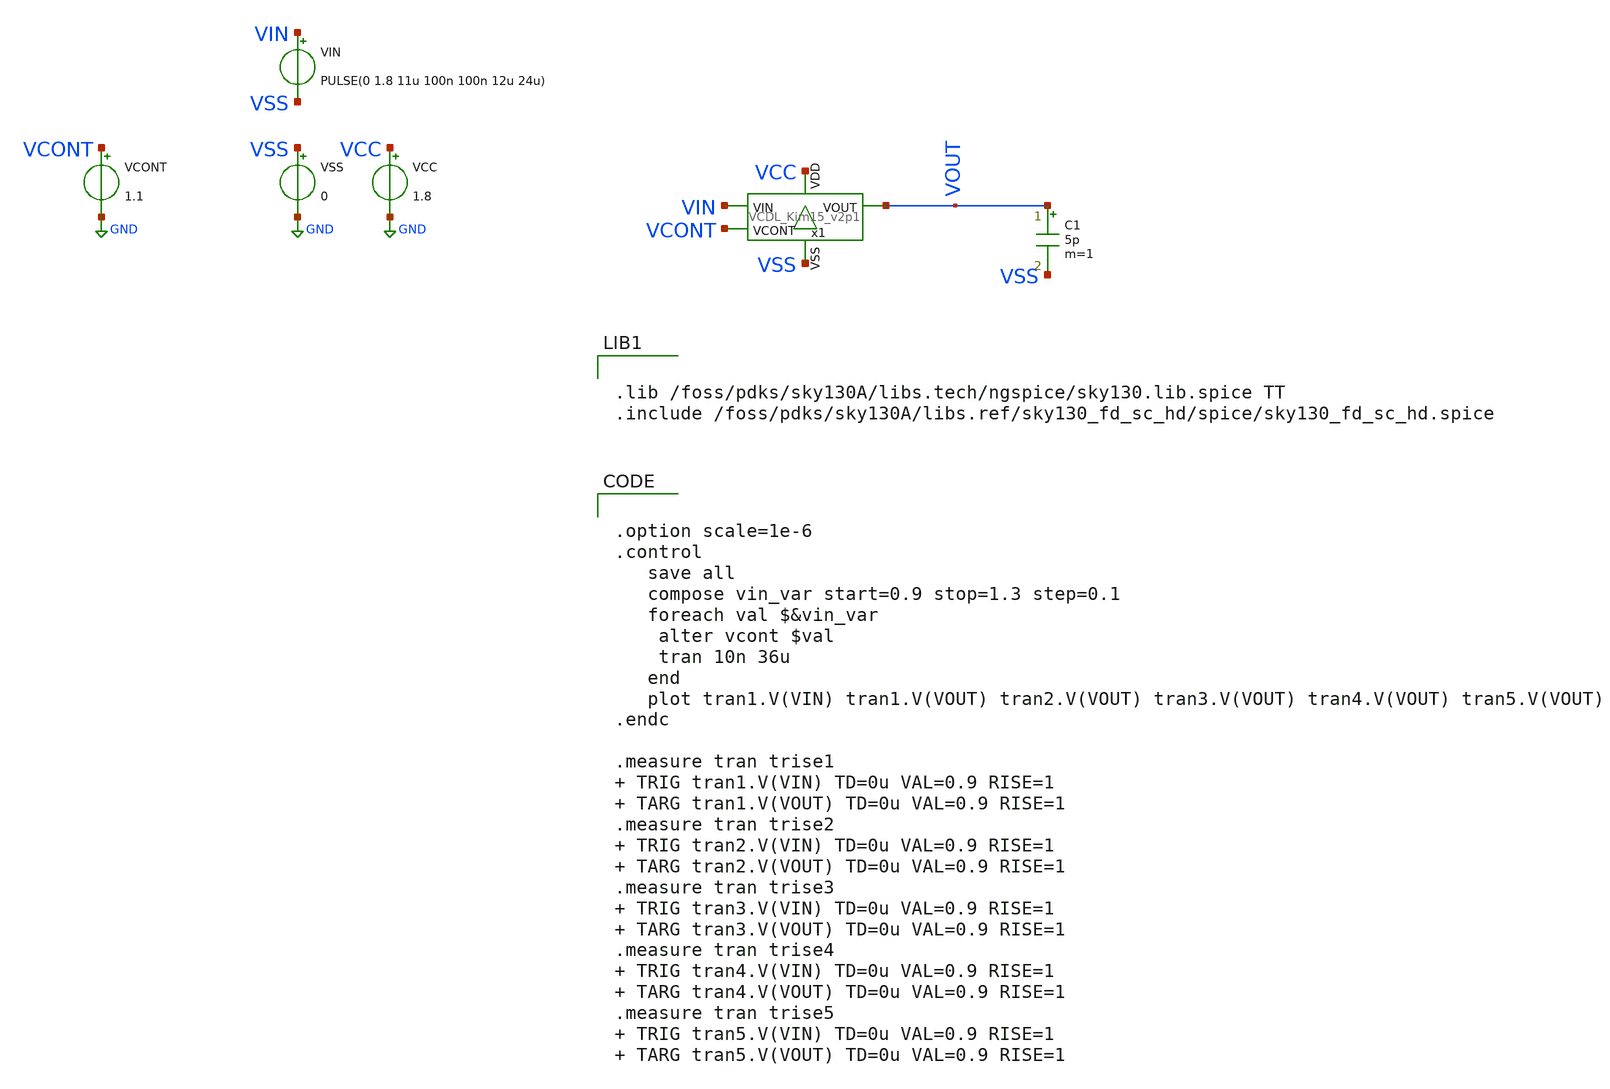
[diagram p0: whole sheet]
** sch_path: xschem/tb_VCDL_Kim_v2p1.sch
**.subckt tb_VCDL_Kim_v2p1
VCC VCC GND 1.8
VSS VSS GND 0
VIN VIN VSS PULSE(0 1.8 11u 100n 100n 12u 24u)
VCONT VCONT GND 1.1
C1 VOUT VSS 5p m=1
x1 VCC VCONT VOUT VIN VSS VCDL_Kim15_v2p1
**** begin user architecture code


.lib /foss/pdks/sky130A/libs.tech/ngspice/sky130.lib.spice TT
.include /foss/pdks/sky130A/libs.ref/sky130_fd_sc_hd/spice/sky130_fd_sc_hd.spice




.option scale=1e-6
.control
   save all
   compose vin_var start=0.9 stop=1.3 step=0.1
   foreach val $&vin_var
	alter vcont $val
	tran 10n 36u
   end
   plot tran1.V(VIN) tran1.V(VOUT) tran2.V(VOUT) tran3.V(VOUT) tran4.V(VOUT) tran5.V(VOUT)
.endc

.measure tran trise1   TRIG tran1.V(VIN) TD=0u VAL=0.9 RISE=1  TARG tran1.V(VOUT) TD=0u VAL=0.9
+ RISE=1
.measure tran trise2  TRIG tran2.V(VIN) TD=0u VAL=0.9 RISE=1  TARG tran2.V(VOUT) TD=0u VAL=0.9
+ RISE=1
.measure tran trise3  TRIG tran3.V(VIN) TD=0u VAL=0.9 RISE=1  TARG tran3.V(VOUT) TD=0u VAL=0.9
+ RISE=1
.measure tran trise4  TRIG tran4.V(VIN) TD=0u VAL=0.9 RISE=1  TARG tran4.V(VOUT) TD=0u VAL=0.9
+ RISE=1
.measure tran trise5  TRIG tran5.V(VIN) TD=0u VAL=0.9 RISE=1  TARG tran5.V(VOUT) TD=0u VAL=0.9
+ RISE=1


**** end user architecture code
**.ends

* expanding   symbol:  /foss/designs/TO202406_CMOSVCO_Esm22/xschem/VCDL_Kim15_v2p1.sym # of pins=5
** sym_path: xschem/VCDL_Kim15_v2p1.sym
** sch_path: xschem/VCDL_Kim15_v2p1.sch
.subckt VCDL_Kim15_v2p1 VDD VCONT VOUT VIN VSS
*.ipin VIN
*.opin VOUT
*.iopin VSS
*.ipin VCONT
*.iopin VDD
XM1 net2 net1 VSS VSS sky130_fd_pr__nfet_01v8 L=5 W=2 nf=1 ad='int((nf+1)/2) * W/nf * 0.29' as='int((nf+2)/2) * W/nf * 0.29'
+ pd='2*int((nf+1)/2) * (W/nf + 0.29)' ps='2*int((nf+2)/2) * (W/nf + 0.29)' nrd='0.29 / W' nrs='0.29 / W'
+ sa=0 sb=0 sd=0 mult=1 m=1
XM2 net2 net1 VCONT VCONT sky130_fd_pr__pfet_01v8 L=5 W=5 nf=1 ad='int((nf+1)/2) * W/nf * 0.29' as='int((nf+2)/2) * W/nf * 0.29'
+ pd='2*int((nf+1)/2) * (W/nf + 0.29)' ps='2*int((nf+2)/2) * (W/nf + 0.29)' nrd='0.29 / W' nrs='0.29 / W'
+ sa=0 sb=0 sd=0 mult=1 m=1
XM3 net3 net2 VSS VSS sky130_fd_pr__nfet_01v8 L=5 W=2 nf=1 ad='int((nf+1)/2) * W/nf * 0.29' as='int((nf+2)/2) * W/nf * 0.29'
+ pd='2*int((nf+1)/2) * (W/nf + 0.29)' ps='2*int((nf+2)/2) * (W/nf + 0.29)' nrd='0.29 / W' nrs='0.29 / W'
+ sa=0 sb=0 sd=0 mult=1 m=1
XM5 net3 net2 VCONT VCONT sky130_fd_pr__pfet_01v8 L=5 W=5 nf=1 ad='int((nf+1)/2) * W/nf * 0.29' as='int((nf+2)/2) * W/nf * 0.29'
+ pd='2*int((nf+1)/2) * (W/nf + 0.29)' ps='2*int((nf+2)/2) * (W/nf + 0.29)' nrd='0.29 / W' nrs='0.29 / W'
+ sa=0 sb=0 sd=0 mult=1 m=1
XM6 net1 net4 VSS VSS sky130_fd_pr__nfet_01v8 L=5 W=2 nf=1 ad='int((nf+1)/2) * W/nf * 0.29' as='int((nf+2)/2) * W/nf * 0.29'
+ pd='2*int((nf+1)/2) * (W/nf + 0.29)' ps='2*int((nf+2)/2) * (W/nf + 0.29)' nrd='0.29 / W' nrs='0.29 / W'
+ sa=0 sb=0 sd=0 mult=1 m=1
XM7 net1 net4 VCONT VCONT sky130_fd_pr__pfet_01v8 L=5 W=5 nf=1 ad='int((nf+1)/2) * W/nf * 0.29' as='int((nf+2)/2) * W/nf * 0.29'
+ pd='2*int((nf+1)/2) * (W/nf + 0.29)' ps='2*int((nf+2)/2) * (W/nf + 0.29)' nrd='0.29 / W' nrs='0.29 / W'
+ sa=0 sb=0 sd=0 mult=1 m=1
XM8 net5 net3 VSS VSS sky130_fd_pr__nfet_01v8 L=5 W=2 nf=1 ad='int((nf+1)/2) * W/nf * 0.29' as='int((nf+2)/2) * W/nf * 0.29'
+ pd='2*int((nf+1)/2) * (W/nf + 0.29)' ps='2*int((nf+2)/2) * (W/nf + 0.29)' nrd='0.29 / W' nrs='0.29 / W'
+ sa=0 sb=0 sd=0 mult=1 m=1
XM9 net5 net3 VCONT VCONT sky130_fd_pr__pfet_01v8 L=5 W=5 nf=1 ad='int((nf+1)/2) * W/nf * 0.29' as='int((nf+2)/2) * W/nf * 0.29'
+ pd='2*int((nf+1)/2) * (W/nf + 0.29)' ps='2*int((nf+2)/2) * (W/nf + 0.29)' nrd='0.29 / W' nrs='0.29 / W'
+ sa=0 sb=0 sd=0 mult=1 m=1
XM4 net6 net5 VSS VSS sky130_fd_pr__nfet_01v8 L=5 W=2 nf=1 ad='int((nf+1)/2) * W/nf * 0.29' as='int((nf+2)/2) * W/nf * 0.29'
+ pd='2*int((nf+1)/2) * (W/nf + 0.29)' ps='2*int((nf+2)/2) * (W/nf + 0.29)' nrd='0.29 / W' nrs='0.29 / W'
+ sa=0 sb=0 sd=0 mult=1 m=1
XM11 net6 net5 VCONT VCONT sky130_fd_pr__pfet_01v8 L=5 W=5 nf=1 ad='int((nf+1)/2) * W/nf * 0.29' as='int((nf+2)/2) * W/nf * 0.29'
+ pd='2*int((nf+1)/2) * (W/nf + 0.29)' ps='2*int((nf+2)/2) * (W/nf + 0.29)' nrd='0.29 / W' nrs='0.29 / W'
+ sa=0 sb=0 sd=0 mult=1 m=1
XM12 net7 net6 VSS VSS sky130_fd_pr__nfet_01v8 L=5 W=2 nf=1 ad='int((nf+1)/2) * W/nf * 0.29' as='int((nf+2)/2) * W/nf * 0.29'
+ pd='2*int((nf+1)/2) * (W/nf + 0.29)' ps='2*int((nf+2)/2) * (W/nf + 0.29)' nrd='0.29 / W' nrs='0.29 / W'
+ sa=0 sb=0 sd=0 mult=1 m=1
XM13 net7 net6 VCONT VCONT sky130_fd_pr__pfet_01v8 L=5 W=5 nf=1 ad='int((nf+1)/2) * W/nf * 0.29' as='int((nf+2)/2) * W/nf * 0.29'
+ pd='2*int((nf+1)/2) * (W/nf + 0.29)' ps='2*int((nf+2)/2) * (W/nf + 0.29)' nrd='0.29 / W' nrs='0.29 / W'
+ sa=0 sb=0 sd=0 mult=1 m=1
XM10 net4 VIN VSS VSS sky130_fd_pr__nfet_01v8 L=5 W=2 nf=1 ad='int((nf+1)/2) * W/nf * 0.29' as='int((nf+2)/2) * W/nf * 0.29'
+ pd='2*int((nf+1)/2) * (W/nf + 0.29)' ps='2*int((nf+2)/2) * (W/nf + 0.29)' nrd='0.29 / W' nrs='0.29 / W'
+ sa=0 sb=0 sd=0 mult=1 m=1
XM14 net4 VIN VDD VDD sky130_fd_pr__pfet_01v8 L=5 W=5 nf=1 ad='int((nf+1)/2) * W/nf * 0.29' as='int((nf+2)/2) * W/nf * 0.29'
+ pd='2*int((nf+1)/2) * (W/nf + 0.29)' ps='2*int((nf+2)/2) * (W/nf + 0.29)' nrd='0.29 / W' nrs='0.29 / W'
+ sa=0 sb=0 sd=0 mult=1 m=1
XM15 VOUT net7 VSS VSS sky130_fd_pr__nfet_01v8 L=5 W=2 nf=1 ad='int((nf+1)/2) * W/nf * 0.29' as='int((nf+2)/2) * W/nf * 0.29'
+ pd='2*int((nf+1)/2) * (W/nf + 0.29)' ps='2*int((nf+2)/2) * (W/nf + 0.29)' nrd='0.29 / W' nrs='0.29 / W'
+ sa=0 sb=0 sd=0 mult=1 m=1
XM16 VOUT net7 VDD VDD sky130_fd_pr__pfet_01v8 L=5 W=5 nf=1 ad='int((nf+1)/2) * W/nf * 0.29' as='int((nf+2)/2) * W/nf * 0.29'
+ pd='2*int((nf+1)/2) * (W/nf + 0.29)' ps='2*int((nf+2)/2) * (W/nf + 0.29)' nrd='0.29 / W' nrs='0.29 / W'
+ sa=0 sb=0 sd=0 mult=1 m=1
.ends

.GLOBAL GND
.end
